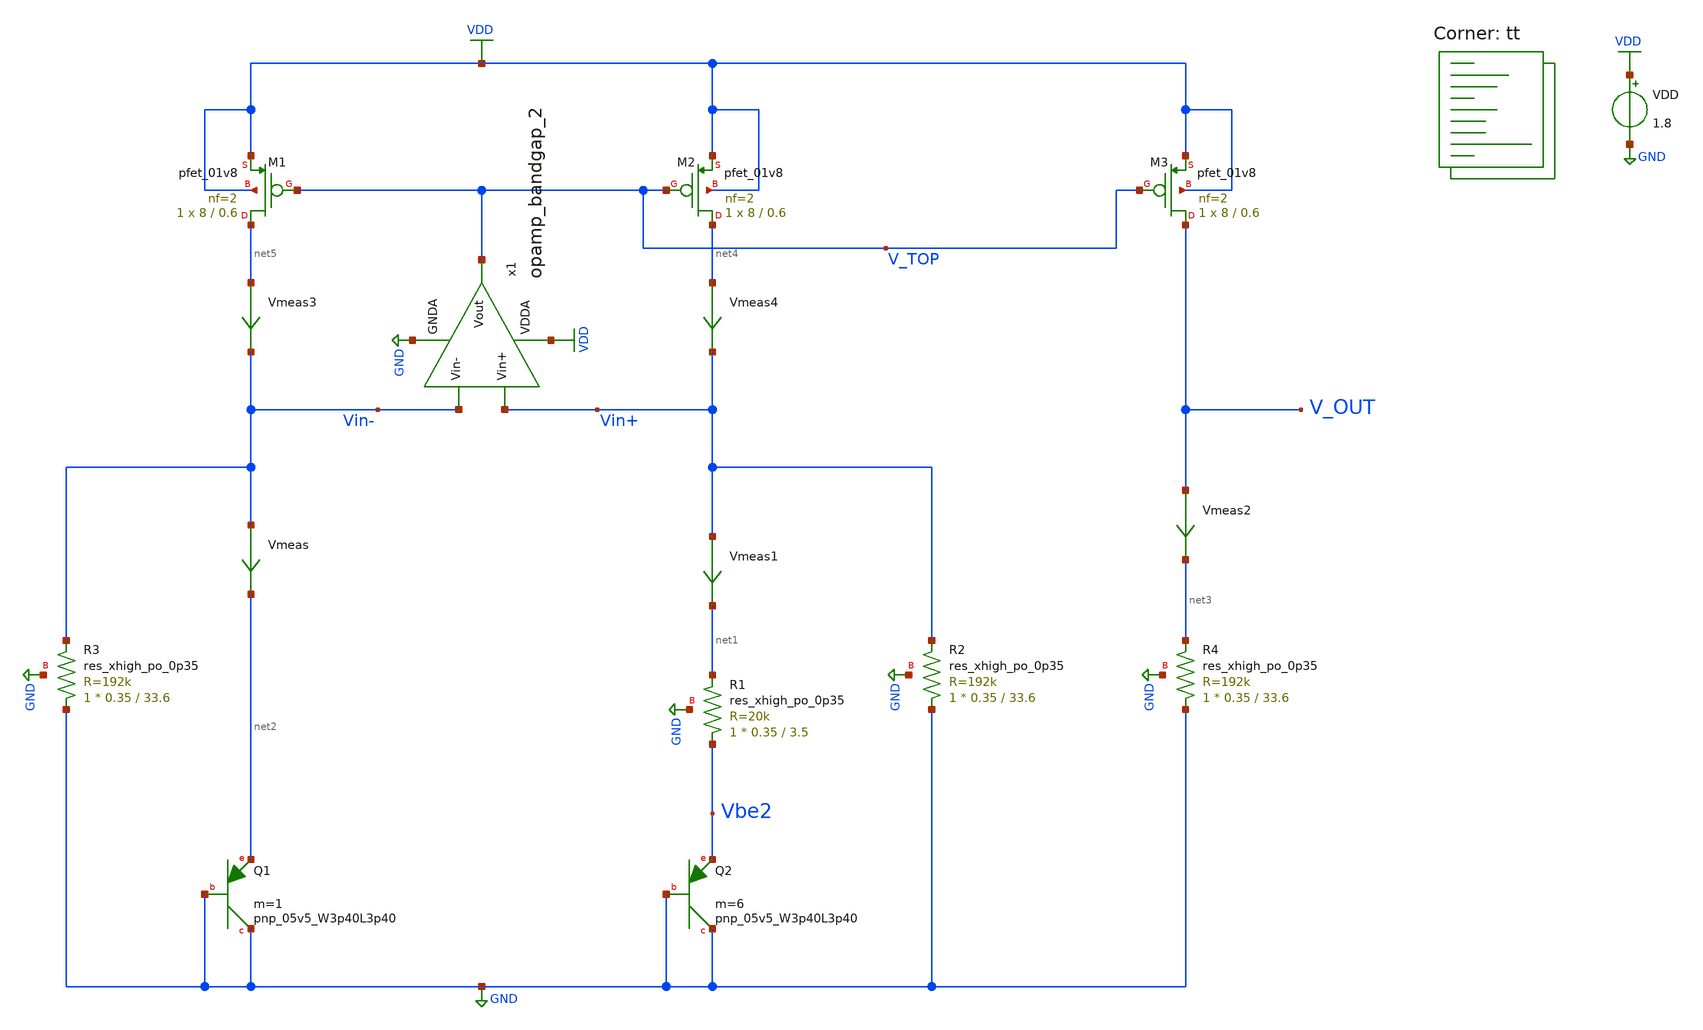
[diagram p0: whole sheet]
** sch_path: projects/bandgapref/xschem_ngspice/new_files/tb_low_voltage_BGR_2.sch
**.subckt tb_low_voltage_BGR_2
VDD VDD GND 1.8
XQ1 GND GND net2 sky130_fd_pr__pnp_05v5_W3p40L3p40 m=1
XQ2 GND GND Vbe2 sky130_fd_pr__pnp_05v5_W3p40L3p40 m=6
XM1 net5 V_TOP VDD VDD sky130_fd_pr__pfet_01v8 L=0.6 W=8 nf=2 ad='int((nf+1)/2) * W/nf * 0.29' as='int((nf+2)/2) * W/nf * 0.29'
+ pd='2*int((nf+1)/2) * (W/nf + 0.29)' ps='2*int((nf+2)/2) * (W/nf + 0.29)' nrd='0.29 / W' nrs='0.29 / W'
+ sa=0 sb=0 sd=0 mult=1 m=1
XM2 net4 V_TOP VDD VDD sky130_fd_pr__pfet_01v8 L=0.6 W=8 nf=2 ad='int((nf+1)/2) * W/nf * 0.29' as='int((nf+2)/2) * W/nf * 0.29'
+ pd='2*int((nf+1)/2) * (W/nf + 0.29)' ps='2*int((nf+2)/2) * (W/nf + 0.29)' nrd='0.29 / W' nrs='0.29 / W'
+ sa=0 sb=0 sd=0 mult=1 m=1
XM3 V_OUT V_TOP VDD VDD sky130_fd_pr__pfet_01v8 L=0.6 W=8 nf=2 ad='int((nf+1)/2) * W/nf * 0.29' as='int((nf+2)/2) * W/nf * 0.29'
+ pd='2*int((nf+1)/2) * (W/nf + 0.29)' ps='2*int((nf+2)/2) * (W/nf + 0.29)' nrd='0.29 / W' nrs='0.29 / W'
+ sa=0 sb=0 sd=0 mult=1 m=1
x1 VDD V_TOP Vin- Vin+ GND opamp_bandgap_2
Vmeas Vin- net2 0
.save i(vmeas)
Vmeas1 Vin+ net1 0
.save i(vmeas1)
Vmeas2 V_OUT net3 0
.save i(vmeas2)
XR1 Vbe2 net1 GND sky130_fd_pr__res_xhigh_po_0p35 L=3.5 mult=1 m=1
XR2 GND Vin+ GND sky130_fd_pr__res_xhigh_po_0p35 L=33.6 mult=1 m=1
XR3 GND Vin- GND sky130_fd_pr__res_xhigh_po_0p35 L=33.6 mult=1 m=1
XR4 GND net3 GND sky130_fd_pr__res_xhigh_po_0p35 L=33.6 mult=1 m=1
Vmeas3 net5 Vin- 0
.save i(vmeas3)
Vmeas4 net4 Vin+ 0
.save i(vmeas4)
**** begin user architecture code
.lib $::SKYWATER_MODELS/sky130.lib.spice tt



.option method=gear
.option wnflag=1
.option savecurrents

.save @m.xm1.msky130_fd_pr__pfet_01v8[gm] @m.xm2.msky130_fd_pr__pfet_01v8[gm] @m.xm3.msky130_fd_pr__pfet_01v8[gm] @m.x1.xm1.msky130_fd_pr__nfet_01v8[gm] @m.x1.xm2.msky130_fd_pr__nfet_01v8[gm] @m.x1.xm3.msky130_fd_pr__nfet_01v8[gm] @m.x1.xm4.msky130_fd_pr__pfet_01v8[gm] @m.x1.xm4.msky130_fd_pr__pfet_01v8[gm]


.control
  save all
  op
  *  dc temp -40 120 1
  * dc temp -40 120 10 VDD 0 4.0 0.2
  dc VDD 0 4.0 0.2 temp -40 120 10
  * tran 1ns 40us
  remzerovec
  write tb_low_voltage_BGR_2.raw
  set appendwrite
.endc




**** end user architecture code
**.ends

* expanding   symbol:  opamp_bandgap_2.sym # of pins=5
** sym_path: projects/bandgapref/xschem_ngspice/new_files/opamp_bandgap_2.sym
** sch_path: projects/bandgapref/xschem_ngspice/new_files/opamp_bandgap_2.sch
.subckt opamp_bandgap_2 VDDA Vout Vin- Vin+ GNDA
*.ipin Vin+
*.opin Vout
*.ipin Vin-
*.ipin GNDA
*.ipin VDDA
XM1 net1 net1 GNDA GNDA sky130_fd_pr__nfet_01v8 L=4 W=4 nf=1 ad='int((nf+1)/2) * W/nf * 0.29' as='int((nf+2)/2) * W/nf * 0.29'
+ pd='2*int((nf+1)/2) * (W/nf + 0.29)' ps='2*int((nf+2)/2) * (W/nf + 0.29)' nrd='0.29 / W' nrs='0.29 / W'
+ sa=0 sb=0 sd=0 mult=1 m=1
XM2 net3 Vin- net1 net1 sky130_fd_pr__nfet_01v8 L=0.6 W=4 nf=1 ad='int((nf+1)/2) * W/nf * 0.29' as='int((nf+2)/2) * W/nf * 0.29'
+ pd='2*int((nf+1)/2) * (W/nf + 0.29)' ps='2*int((nf+2)/2) * (W/nf + 0.29)' nrd='0.29 / W' nrs='0.29 / W'
+ sa=0 sb=0 sd=0 mult=1 m=1
XM3 net2 Vin+ net1 net1 sky130_fd_pr__nfet_01v8 L=0.6 W=4 nf=1 ad='int((nf+1)/2) * W/nf * 0.29' as='int((nf+2)/2) * W/nf * 0.29'
+ pd='2*int((nf+1)/2) * (W/nf + 0.29)' ps='2*int((nf+2)/2) * (W/nf + 0.29)' nrd='0.29 / W' nrs='0.29 / W'
+ sa=0 sb=0 sd=0 mult=1 m=1
XM4 net3 net3 VDDA VDDA sky130_fd_pr__pfet_01v8 L=0.6 W=8 nf=2 ad='int((nf+1)/2) * W/nf * 0.29' as='int((nf+2)/2) * W/nf * 0.29'
+ pd='2*int((nf+1)/2) * (W/nf + 0.29)' ps='2*int((nf+2)/2) * (W/nf + 0.29)' nrd='0.29 / W' nrs='0.29 / W'
+ sa=0 sb=0 sd=0 mult=1 m=1
XM5 net2 net3 VDDA VDDA sky130_fd_pr__pfet_01v8 L=0.6 W=8 nf=2 ad='int((nf+1)/2) * W/nf * 0.29' as='int((nf+2)/2) * W/nf * 0.29'
+ pd='2*int((nf+1)/2) * (W/nf + 0.29)' ps='2*int((nf+2)/2) * (W/nf + 0.29)' nrd='0.29 / W' nrs='0.29 / W'
+ sa=0 sb=0 sd=0 mult=1 m=1
XM6 Vout Vout GNDA GNDA sky130_fd_pr__nfet_01v8 L=4 W=4 nf=1 ad='int((nf+1)/2) * W/nf * 0.29' as='int((nf+2)/2) * W/nf * 0.29'
+ pd='2*int((nf+1)/2) * (W/nf + 0.29)' ps='2*int((nf+2)/2) * (W/nf + 0.29)' nrd='0.29 / W' nrs='0.29 / W'
+ sa=0 sb=0 sd=0 mult=1 m=1
XM7 Vout net2 VDDA VDDA sky130_fd_pr__pfet_01v8 L=0.6 W=8 nf=2 ad='int((nf+1)/2) * W/nf * 0.29' as='int((nf+2)/2) * W/nf * 0.29'
+ pd='2*int((nf+1)/2) * (W/nf + 0.29)' ps='2*int((nf+2)/2) * (W/nf + 0.29)' nrd='0.29 / W' nrs='0.29 / W'
+ sa=0 sb=0 sd=0 mult=1 m=1
.ends

.GLOBAL GND
.GLOBAL VDD
.end
